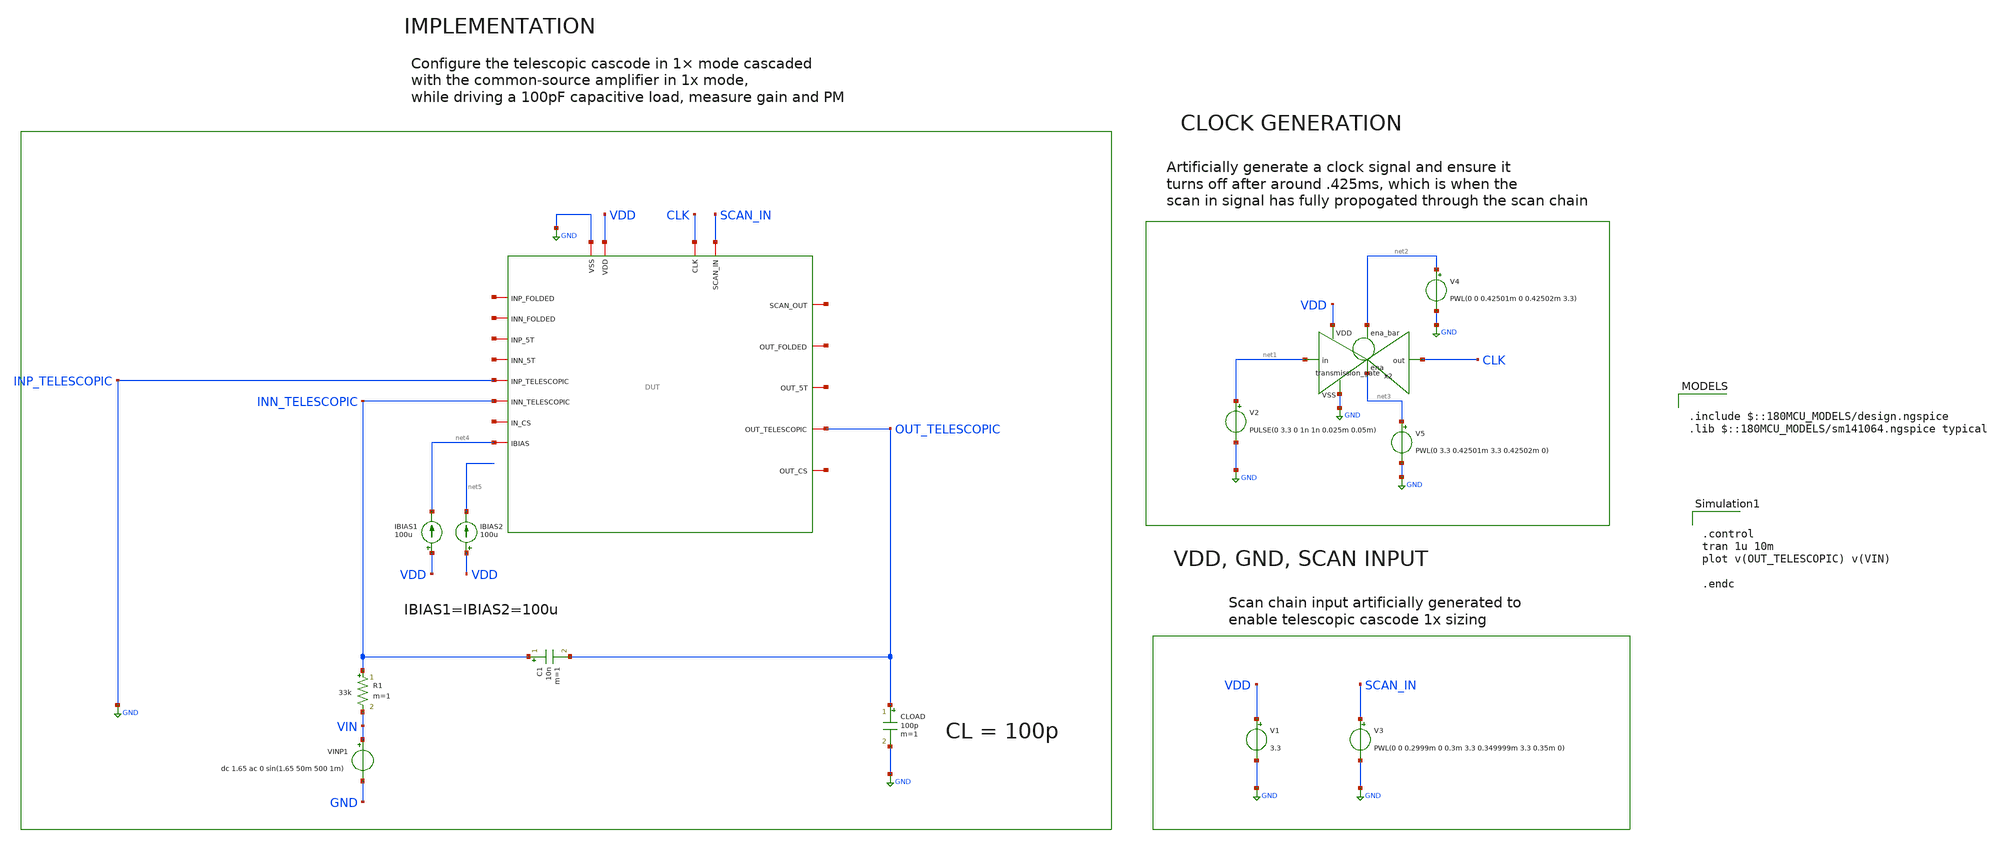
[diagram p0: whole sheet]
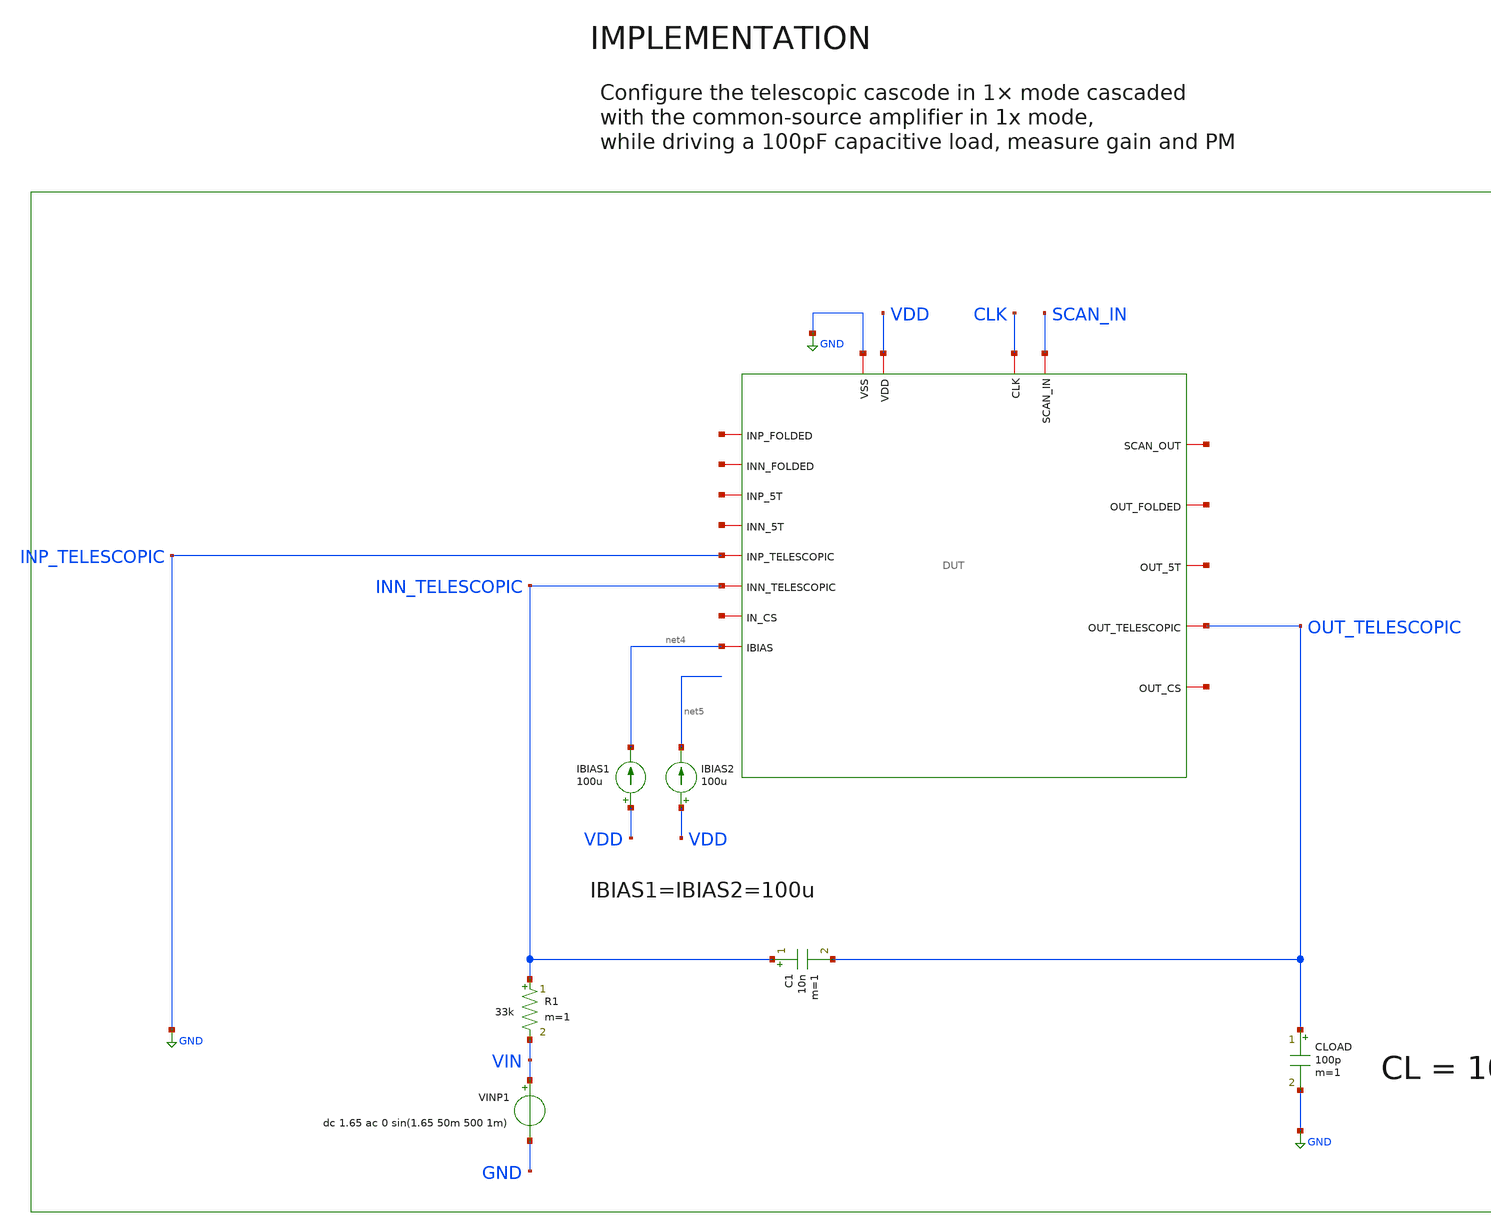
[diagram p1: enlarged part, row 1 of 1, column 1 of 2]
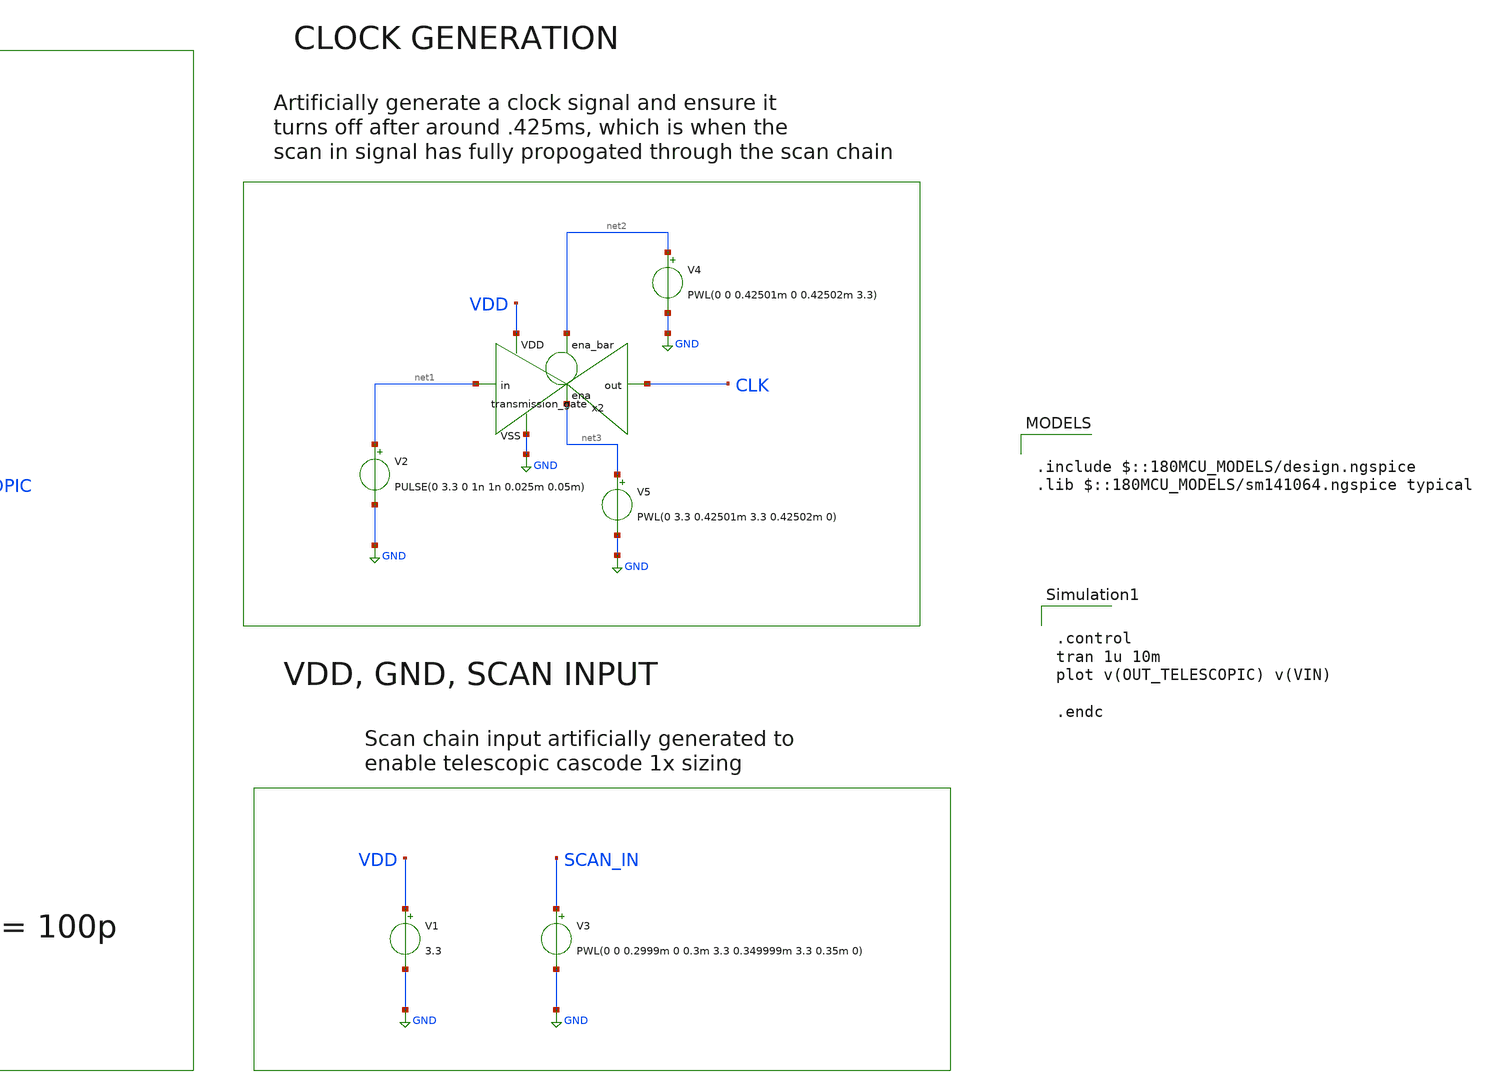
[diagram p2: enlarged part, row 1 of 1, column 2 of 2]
** sch_path: designs/untitled-5.sch
**.subckt untitled-5
V3 SCAN_IN GND PWL(0 0 0.2999m 0 0.3m 3.3 0.349999m 3.3 0.35m 0)
V1 VDD GND 3.3
V2 net1 GND PULSE(0 3.3 0 1n 1n 0.025m 0.05m)
x2 net2 VDD CLK net1 GND net3 transmission_gate
V4 net2 GND PWL(0 0 0.42501m 0 0.42502m 3.3)
V5 net3 GND PWL(0 3.3 0.42501m 3.3 0.42502m 0)
IBIAS1 VDD net4 100u
IBIAS2 VDD net5 100u
CLOAD OUT_TELESCOPIC GND 100p m=1
x1 CLK net6 SCAN_IN GND VDD net7 net8 net9 net4 net10 net11 net12 INP_TELESCOPIC OUT_TELESCOPIC
+ net13 net14 INN_TELESCOPIC DUT
VINP1 VIN GND dc 1.65 ac 0 sin(1.65 50m 500 1m)
C1 INN_TELESCOPIC OUT_TELESCOPIC 10n m=1
R1 INN_TELESCOPIC VIN 33k m=1
**** begin user architecture code

.include $::180MCU_MODELS/design.ngspice
.lib $::180MCU_MODELS/sm141064.ngspice typical



.control
tran 1u 10m
plot v(OUT_TELESCOPIC) v(VIN)

.endc


**** end user architecture code
**.ends
.GLOBAL GND
.end
